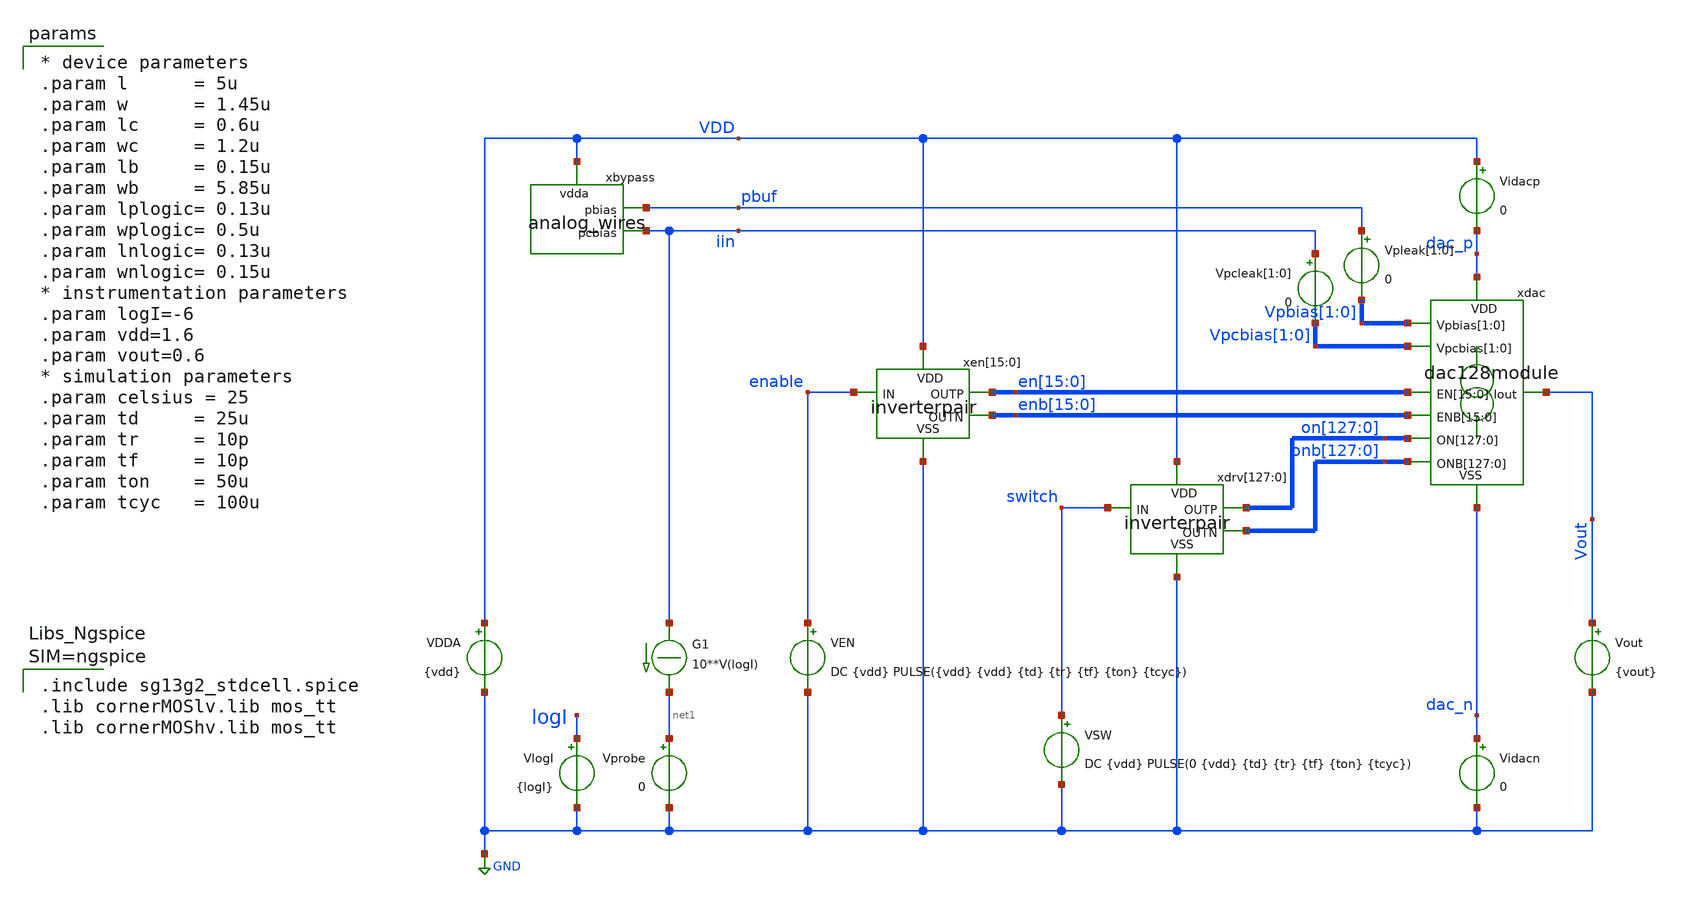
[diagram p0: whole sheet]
** sch_path: xschem/test_dac128_dc.sch
**.subckt test_dac128_dc
Vout Vout GND {vout}
.save i(vout)
Vprobe net1 GND 0
.save i(vprobe)
G1 iin net1 CUR=' 10**V(logI) '
VlogI logI GND {logI}
.save i(vlogi)
VDDA VDD GND {vdd}
.save i(vdda)
VSW switch GND DC {vdd} PULSE(0 {vdd} {td} {tr} {tf} {ton} {tcyc})
.save i(vsw)
Vidacp VDD dac_p 0
.save i(vidacp)
Vidacn dac_n GND 0
.save i(vidacn)
Vpleak[1] pbuf Vpbias[1] 0
Vpleak[0] pbuf Vpbias[0] 0
.save i(vpleak[1])
.save i(vpleak[0])
xdac dac_p en[15] en[14] en[13] en[12] en[11] en[10] en[9] en[8] en[7] en[6] en[5] en[4] en[3] en[2]
+ en[1] en[0] enb[15] enb[14] enb[13] enb[12] enb[11] enb[10] enb[9] enb[8] enb[7] enb[6] enb[5] enb[4]
+ enb[3] enb[2] enb[1] enb[0] on[127] on[126] on[125] on[124] on[123] on[122] on[121] on[120] on[119]
+ on[118] on[117] on[116] on[115] on[114] on[113] on[112] on[111] on[110] on[109] on[108] on[107] on[106]
+ on[105] on[104] on[103] on[102] on[101] on[100] on[99] on[98] on[97] on[96] on[95] on[94] on[93] on[92]
+ on[91] on[90] on[89] on[88] on[87] on[86] on[85] on[84] on[83] on[82] on[81] on[80] on[79] on[78] on[77]
+ on[76] on[75] on[74] on[73] on[72] on[71] on[70] on[69] on[68] on[67] on[66] on[65] on[64] on[63] on[62]
+ on[61] on[60] on[59] on[58] on[57] on[56] on[55] on[54] on[53] on[52] on[51] on[50] on[49] on[48] on[47]
+ on[46] on[45] on[44] on[43] on[42] on[41] on[40] on[39] on[38] on[37] on[36] on[35] on[34] on[33] on[32]
+ on[31] on[30] on[29] on[28] on[27] on[26] on[25] on[24] on[23] on[22] on[21] on[20] on[19] on[18] on[17]
+ on[16] on[15] on[14] on[13] on[12] on[11] on[10] on[9] on[8] on[7] on[6] on[5] on[4] on[3] on[2] on[1]
+ on[0] onb[127] onb[126] onb[125] onb[124] onb[123] onb[122] onb[121] onb[120] onb[119] onb[118] onb[117]
+ onb[116] onb[115] onb[114] onb[113] onb[112] onb[111] onb[110] onb[109] onb[108] onb[107] onb[106] onb[105]
+ onb[104] onb[103] onb[102] onb[101] onb[100] onb[99] onb[98] onb[97] onb[96] onb[95] onb[94] onb[93] onb[92]
+ onb[91] onb[90] onb[89] onb[88] onb[87] onb[86] onb[85] onb[84] onb[83] onb[82] onb[81] onb[80] onb[79]
+ onb[78] onb[77] onb[76] onb[75] onb[74] onb[73] onb[72] onb[71] onb[70] onb[69] onb[68] onb[67] onb[66]
+ onb[65] onb[64] onb[63] onb[62] onb[61] onb[60] onb[59] onb[58] onb[57] onb[56] onb[55] onb[54] onb[53]
+ onb[52] onb[51] onb[50] onb[49] onb[48] onb[47] onb[46] onb[45] onb[44] onb[43] onb[42] onb[41] onb[40]
+ onb[39] onb[38] onb[37] onb[36] onb[35] onb[34] onb[33] onb[32] onb[31] onb[30] onb[29] onb[28] onb[27]
+ onb[26] onb[25] onb[24] onb[23] onb[22] onb[21] onb[20] onb[19] onb[18] onb[17] onb[16] onb[15] onb[14]
+ onb[13] onb[12] onb[11] onb[10] onb[9] onb[8] onb[7] onb[6] onb[5] onb[4] onb[3] onb[2] onb[1] onb[0] Vout
+ Vpbias[1] Vpbias[0] Vpcbias[1] Vpcbias[0] dac_n dac128module
xbypass VDD pbuf iin analog_wires
Vpcleak[1] iin Vpcbias[1] 0
Vpcleak[0] iin Vpcbias[0] 0
.save i(vpcleak[1])
.save i(vpcleak[0])
xen[15] VDD en[15] enable enb[15] GND inverterpair
xen[14] VDD en[14] enable enb[14] GND inverterpair
xen[13] VDD en[13] enable enb[13] GND inverterpair
xen[12] VDD en[12] enable enb[12] GND inverterpair
xen[11] VDD en[11] enable enb[11] GND inverterpair
xen[10] VDD en[10] enable enb[10] GND inverterpair
xen[9] VDD en[9] enable enb[9] GND inverterpair
xen[8] VDD en[8] enable enb[8] GND inverterpair
xen[7] VDD en[7] enable enb[7] GND inverterpair
xen[6] VDD en[6] enable enb[6] GND inverterpair
xen[5] VDD en[5] enable enb[5] GND inverterpair
xen[4] VDD en[4] enable enb[4] GND inverterpair
xen[3] VDD en[3] enable enb[3] GND inverterpair
xen[2] VDD en[2] enable enb[2] GND inverterpair
xen[1] VDD en[1] enable enb[1] GND inverterpair
xen[0] VDD en[0] enable enb[0] GND inverterpair
xdrv[127] VDD on[127] switch onb[127] GND inverterpair
xdrv[126] VDD on[126] switch onb[126] GND inverterpair
xdrv[125] VDD on[125] switch onb[125] GND inverterpair
xdrv[124] VDD on[124] switch onb[124] GND inverterpair
xdrv[123] VDD on[123] switch onb[123] GND inverterpair
xdrv[122] VDD on[122] switch onb[122] GND inverterpair
xdrv[121] VDD on[121] switch onb[121] GND inverterpair
xdrv[120] VDD on[120] switch onb[120] GND inverterpair
xdrv[119] VDD on[119] switch onb[119] GND inverterpair
xdrv[118] VDD on[118] switch onb[118] GND inverterpair
xdrv[117] VDD on[117] switch onb[117] GND inverterpair
xdrv[116] VDD on[116] switch onb[116] GND inverterpair
xdrv[115] VDD on[115] switch onb[115] GND inverterpair
xdrv[114] VDD on[114] switch onb[114] GND inverterpair
xdrv[113] VDD on[113] switch onb[113] GND inverterpair
xdrv[112] VDD on[112] switch onb[112] GND inverterpair
xdrv[111] VDD on[111] switch onb[111] GND inverterpair
xdrv[110] VDD on[110] switch onb[110] GND inverterpair
xdrv[109] VDD on[109] switch onb[109] GND inverterpair
xdrv[108] VDD on[108] switch onb[108] GND inverterpair
xdrv[107] VDD on[107] switch onb[107] GND inverterpair
xdrv[106] VDD on[106] switch onb[106] GND inverterpair
xdrv[105] VDD on[105] switch onb[105] GND inverterpair
xdrv[104] VDD on[104] switch onb[104] GND inverterpair
xdrv[103] VDD on[103] switch onb[103] GND inverterpair
xdrv[102] VDD on[102] switch onb[102] GND inverterpair
xdrv[101] VDD on[101] switch onb[101] GND inverterpair
xdrv[100] VDD on[100] switch onb[100] GND inverterpair
xdrv[99] VDD on[99] switch onb[99] GND inverterpair
xdrv[98] VDD on[98] switch onb[98] GND inverterpair
xdrv[97] VDD on[97] switch onb[97] GND inverterpair
xdrv[96] VDD on[96] switch onb[96] GND inverterpair
xdrv[95] VDD on[95] switch onb[95] GND inverterpair
xdrv[94] VDD on[94] switch onb[94] GND inverterpair
xdrv[93] VDD on[93] switch onb[93] GND inverterpair
xdrv[92] VDD on[92] switch onb[92] GND inverterpair
xdrv[91] VDD on[91] switch onb[91] GND inverterpair
xdrv[90] VDD on[90] switch onb[90] GND inverterpair
xdrv[89] VDD on[89] switch onb[89] GND inverterpair
xdrv[88] VDD on[88] switch onb[88] GND inverterpair
xdrv[87] VDD on[87] switch onb[87] GND inverterpair
xdrv[86] VDD on[86] switch onb[86] GND inverterpair
xdrv[85] VDD on[85] switch onb[85] GND inverterpair
xdrv[84] VDD on[84] switch onb[84] GND inverterpair
xdrv[83] VDD on[83] switch onb[83] GND inverterpair
xdrv[82] VDD on[82] switch onb[82] GND inverterpair
xdrv[81] VDD on[81] switch onb[81] GND inverterpair
xdrv[80] VDD on[80] switch onb[80] GND inverterpair
xdrv[79] VDD on[79] switch onb[79] GND inverterpair
xdrv[78] VDD on[78] switch onb[78] GND inverterpair
xdrv[77] VDD on[77] switch onb[77] GND inverterpair
xdrv[76] VDD on[76] switch onb[76] GND inverterpair
xdrv[75] VDD on[75] switch onb[75] GND inverterpair
xdrv[74] VDD on[74] switch onb[74] GND inverterpair
xdrv[73] VDD on[73] switch onb[73] GND inverterpair
xdrv[72] VDD on[72] switch onb[72] GND inverterpair
xdrv[71] VDD on[71] switch onb[71] GND inverterpair
xdrv[70] VDD on[70] switch onb[70] GND inverterpair
xdrv[69] VDD on[69] switch onb[69] GND inverterpair
xdrv[68] VDD on[68] switch onb[68] GND inverterpair
xdrv[67] VDD on[67] switch onb[67] GND inverterpair
xdrv[66] VDD on[66] switch onb[66] GND inverterpair
xdrv[65] VDD on[65] switch onb[65] GND inverterpair
xdrv[64] VDD on[64] switch onb[64] GND inverterpair
xdrv[63] VDD on[63] switch onb[63] GND inverterpair
xdrv[62] VDD on[62] switch onb[62] GND inverterpair
xdrv[61] VDD on[61] switch onb[61] GND inverterpair
xdrv[60] VDD on[60] switch onb[60] GND inverterpair
xdrv[59] VDD on[59] switch onb[59] GND inverterpair
xdrv[58] VDD on[58] switch onb[58] GND inverterpair
xdrv[57] VDD on[57] switch onb[57] GND inverterpair
xdrv[56] VDD on[56] switch onb[56] GND inverterpair
xdrv[55] VDD on[55] switch onb[55] GND inverterpair
xdrv[54] VDD on[54] switch onb[54] GND inverterpair
xdrv[53] VDD on[53] switch onb[53] GND inverterpair
xdrv[52] VDD on[52] switch onb[52] GND inverterpair
xdrv[51] VDD on[51] switch onb[51] GND inverterpair
xdrv[50] VDD on[50] switch onb[50] GND inverterpair
xdrv[49] VDD on[49] switch onb[49] GND inverterpair
xdrv[48] VDD on[48] switch onb[48] GND inverterpair
xdrv[47] VDD on[47] switch onb[47] GND inverterpair
xdrv[46] VDD on[46] switch onb[46] GND inverterpair
xdrv[45] VDD on[45] switch onb[45] GND inverterpair
xdrv[44] VDD on[44] switch onb[44] GND inverterpair
xdrv[43] VDD on[43] switch onb[43] GND inverterpair
xdrv[42] VDD on[42] switch onb[42] GND inverterpair
xdrv[41] VDD on[41] switch onb[41] GND inverterpair
xdrv[40] VDD on[40] switch onb[40] GND inverterpair
xdrv[39] VDD on[39] switch onb[39] GND inverterpair
xdrv[38] VDD on[38] switch onb[38] GND inverterpair
xdrv[37] VDD on[37] switch onb[37] GND inverterpair
xdrv[36] VDD on[36] switch onb[36] GND inverterpair
xdrv[35] VDD on[35] switch onb[35] GND inverterpair
xdrv[34] VDD on[34] switch onb[34] GND inverterpair
xdrv[33] VDD on[33] switch onb[33] GND inverterpair
xdrv[32] VDD on[32] switch onb[32] GND inverterpair
xdrv[31] VDD on[31] switch onb[31] GND inverterpair
xdrv[30] VDD on[30] switch onb[30] GND inverterpair
xdrv[29] VDD on[29] switch onb[29] GND inverterpair
xdrv[28] VDD on[28] switch onb[28] GND inverterpair
xdrv[27] VDD on[27] switch onb[27] GND inverterpair
xdrv[26] VDD on[26] switch onb[26] GND inverterpair
xdrv[25] VDD on[25] switch onb[25] GND inverterpair
xdrv[24] VDD on[24] switch onb[24] GND inverterpair
xdrv[23] VDD on[23] switch onb[23] GND inverterpair
xdrv[22] VDD on[22] switch onb[22] GND inverterpair
xdrv[21] VDD on[21] switch onb[21] GND inverterpair
xdrv[20] VDD on[20] switch onb[20] GND inverterpair
xdrv[19] VDD on[19] switch onb[19] GND inverterpair
xdrv[18] VDD on[18] switch onb[18] GND inverterpair
xdrv[17] VDD on[17] switch onb[17] GND inverterpair
xdrv[16] VDD on[16] switch onb[16] GND inverterpair
xdrv[15] VDD on[15] switch onb[15] GND inverterpair
xdrv[14] VDD on[14] switch onb[14] GND inverterpair
xdrv[13] VDD on[13] switch onb[13] GND inverterpair
xdrv[12] VDD on[12] switch onb[12] GND inverterpair
xdrv[11] VDD on[11] switch onb[11] GND inverterpair
xdrv[10] VDD on[10] switch onb[10] GND inverterpair
xdrv[9] VDD on[9] switch onb[9] GND inverterpair
xdrv[8] VDD on[8] switch onb[8] GND inverterpair
xdrv[7] VDD on[7] switch onb[7] GND inverterpair
xdrv[6] VDD on[6] switch onb[6] GND inverterpair
xdrv[5] VDD on[5] switch onb[5] GND inverterpair
xdrv[4] VDD on[4] switch onb[4] GND inverterpair
xdrv[3] VDD on[3] switch onb[3] GND inverterpair
xdrv[2] VDD on[2] switch onb[2] GND inverterpair
xdrv[1] VDD on[1] switch onb[1] GND inverterpair
xdrv[0] VDD on[0] switch onb[0] GND inverterpair
VEN enable GND DC {vdd} PULSE({vdd} {vdd} {td} {tr} {tf} {ton} {tcyc})
.save i(ven)
**** begin user architecture code


.include test_dac128_dc.save
.temp=27
.options gmin=1e-15 abstol=1p method=gear
.options savecurrents
.control
save all
op
write test_dac128_dc.raw
set appendwrite
dc Vout 0 1.6 10m VlogI -7 -5 0.5
*tran 10n 500u
write test_dac128_dc.raw
plot 2*(vout#branch-8*vprobe#branch)/(8*vprobe#branch+vout#branch)
plot vdd pbuf iin enable switch v("en[0]") v("enb[0]") v("on[0]") v("onb[0]") Vout
plot vout#branch vprobe#branch
*plot @n.xsw.xmbias.nsg13_lv_pmos[ids] @n.xsw.xmpullup.nsg13_lv_pmos[ids]
plot vidacp#branch vidacn#branch
*plot 0.5*(vidacp#branch+vidacn#branch) vidacp#branch-vidacn#branch
.endc




.include sg13g2_stdcell.spice
.lib cornerMOSlv.lib mos_tt
.lib cornerMOShv.lib mos_tt



* device parameters
.param l      = 5u
.param w      = 1.45u
.param lc     = 0.6u
.param wc     = 1.2u
.param lb     = 0.15u
.param wb     = 5.85u
.param lplogic= 0.13u
.param wplogic= 0.5u
.param lnlogic= 0.13u
.param wnlogic= 0.15u
* instrumentation parameters
.param logI=-6
.param vdd=1.6
.param vout=0.6
* simulation parameters
.param celsius = 25
.param td     = 25u
.param tr     = 10p
.param tf     = 10p
.param ton    = 50u
.param tcyc   = 100u


**** end user architecture code
**.ends

* expanding   symbol:  dac128module.sym # of pins=9
** sym_path: xschem/dac128module.sym
** sch_path: xschem/dac128module.sch
.subckt dac128module VDD EN[15] EN[14] EN[13] EN[12] EN[11] EN[10] EN[9] EN[8] EN[7] EN[6] EN[5]
+ EN[4] EN[3] EN[2] EN[1] EN[0] ENB[15] ENB[14] ENB[13] ENB[12] ENB[11] ENB[10] ENB[9] ENB[8] ENB[7] ENB[6]
+ ENB[5] ENB[4] ENB[3] ENB[2] ENB[1] ENB[0] ON[127] ON[126] ON[125] ON[124] ON[123] ON[122] ON[121] ON[120]
+ ON[119] ON[118] ON[117] ON[116] ON[115] ON[114] ON[113] ON[112] ON[111] ON[110] ON[109] ON[108] ON[107]
+ ON[106] ON[105] ON[104] ON[103] ON[102] ON[101] ON[100] ON[99] ON[98] ON[97] ON[96] ON[95] ON[94] ON[93]
+ ON[92] ON[91] ON[90] ON[89] ON[88] ON[87] ON[86] ON[85] ON[84] ON[83] ON[82] ON[81] ON[80] ON[79] ON[78]
+ ON[77] ON[76] ON[75] ON[74] ON[73] ON[72] ON[71] ON[70] ON[69] ON[68] ON[67] ON[66] ON[65] ON[64] ON[63]
+ ON[62] ON[61] ON[60] ON[59] ON[58] ON[57] ON[56] ON[55] ON[54] ON[53] ON[52] ON[51] ON[50] ON[49] ON[48]
+ ON[47] ON[46] ON[45] ON[44] ON[43] ON[42] ON[41] ON[40] ON[39] ON[38] ON[37] ON[36] ON[35] ON[34] ON[33]
+ ON[32] ON[31] ON[30] ON[29] ON[28] ON[27] ON[26] ON[25] ON[24] ON[23] ON[22] ON[21] ON[20] ON[19] ON[18]
+ ON[17] ON[16] ON[15] ON[14] ON[13] ON[12] ON[11] ON[10] ON[9] ON[8] ON[7] ON[6] ON[5] ON[4] ON[3] ON[2]
+ ON[1] ON[0] ONB[127] ONB[126] ONB[125] ONB[124] ONB[123] ONB[122] ONB[121] ONB[120] ONB[119] ONB[118]
+ ONB[117] ONB[116] ONB[115] ONB[114] ONB[113] ONB[112] ONB[111] ONB[110] ONB[109] ONB[108] ONB[107] ONB[106]
+ ONB[105] ONB[104] ONB[103] ONB[102] ONB[101] ONB[100] ONB[99] ONB[98] ONB[97] ONB[96] ONB[95] ONB[94]
+ ONB[93] ONB[92] ONB[91] ONB[90] ONB[89] ONB[88] ONB[87] ONB[86] ONB[85] ONB[84] ONB[83] ONB[82] ONB[81]
+ ONB[80] ONB[79] ONB[78] ONB[77] ONB[76] ONB[75] ONB[74] ONB[73] ONB[72] ONB[71] ONB[70] ONB[69] ONB[68]
+ ONB[67] ONB[66] ONB[65] ONB[64] ONB[63] ONB[62] ONB[61] ONB[60] ONB[59] ONB[58] ONB[57] ONB[56] ONB[55]
+ ONB[54] ONB[53] ONB[52] ONB[51] ONB[50] ONB[49] ONB[48] ONB[47] ONB[46] ONB[45] ONB[44] ONB[43] ONB[42]
+ ONB[41] ONB[40] ONB[39] ONB[38] ONB[37] ONB[36] ONB[35] ONB[34] ONB[33] ONB[32] ONB[31] ONB[30] ONB[29]
+ ONB[28] ONB[27] ONB[26] ONB[25] ONB[24] ONB[23] ONB[22] ONB[21] ONB[20] ONB[19] ONB[18] ONB[17] ONB[16]
+ ONB[15] ONB[14] ONB[13] ONB[12] ONB[11] ONB[10] ONB[9] ONB[8] ONB[7] ONB[6] ONB[5] ONB[4] ONB[3] ONB[2]
+ ONB[1] ONB[0] Iout Vpbias[1] Vpbias[0] Vpcbias[1] Vpcbias[0] VSS
*.opin Iout
*.ipin
*+ ON[127],ON[126],ON[125],ON[124],ON[123],ON[122],ON[121],ON[120],ON[119],ON[118],ON[117],ON[116],ON[115],ON[114],ON[113],ON[112],ON[111],ON[110],ON[109],ON[108],ON[107],ON[106],ON[105],ON[104],ON[103],ON[102],ON[101],ON[100],ON[99],ON[98],ON[97],ON[96],ON[95],ON[94],ON[93],ON[92],ON[91],ON[90],ON[89],ON[88],ON[87],ON[86],ON[85],ON[84],ON[83],ON[82],ON[81],ON[80],ON[79],ON[78],ON[77],ON[76],ON[75],ON[74],ON[73],ON[72],ON[71],ON[70],ON[69],ON[68],ON[67],ON[66],ON[65],ON[64],ON[63],ON[62],ON[61],ON[60],ON[59],ON[58],ON[57],ON[56],ON[55],ON[54],ON[53],ON[52],ON[51],ON[50],ON[49],ON[48],ON[47],ON[46],ON[45],ON[44],ON[43],ON[42],ON[41],ON[40],ON[39],ON[38],ON[37],ON[36],ON[35],ON[34],ON[33],ON[32],ON[31],ON[30],ON[29],ON[28],ON[27],ON[26],ON[25],ON[24],ON[23],ON[22],ON[21],ON[20],ON[19],ON[18],ON[17],ON[16],ON[15],ON[14],ON[13],ON[12],ON[11],ON[10],ON[9],ON[8],ON[7],ON[6],ON[5],ON[4],ON[3],ON[2],ON[1],ON[0]
*.ipin
*+ ONB[127],ONB[126],ONB[125],ONB[124],ONB[123],ONB[122],ONB[121],ONB[120],ONB[119],ONB[118],ONB[117],ONB[116],ONB[115],ONB[114],ONB[113],ONB[112],ONB[111],ONB[110],ONB[109],ONB[108],ONB[107],ONB[106],ONB[105],ONB[104],ONB[103],ONB[102],ONB[101],ONB[100],ONB[99],ONB[98],ONB[97],ONB[96],ONB[95],ONB[94],ONB[93],ONB[92],ONB[91],ONB[90],ONB[89],ONB[88],ONB[87],ONB[86],ONB[85],ONB[84],ONB[83],ONB[82],ONB[81],ONB[80],ONB[79],ONB[78],ONB[77],ONB[76],ONB[75],ONB[74],ONB[73],ONB[72],ONB[71],ONB[70],ONB[69],ONB[68],ONB[67],ONB[66],ONB[65],ONB[64],ONB[63],ONB[62],ONB[61],ONB[60],ONB[59],ONB[58],ONB[57],ONB[56],ONB[55],ONB[54],ONB[53],ONB[52],ONB[51],ONB[50],ONB[49],ONB[48],ONB[47],ONB[46],ONB[45],ONB[44],ONB[43],ONB[42],ONB[41],ONB[40],ONB[39],ONB[38],ONB[37],ONB[36],ONB[35],ONB[34],ONB[33],ONB[32],ONB[31],ONB[30],ONB[29],ONB[28],ONB[27],ONB[26],ONB[25],ONB[24],ONB[23],ONB[22],ONB[21],ONB[20],ONB[19],ONB[18],ONB[17],ONB[16],ONB[15],ONB[14],ONB[13],ONB[12],ONB[11],ONB[10],ONB[9],ONB[8],ONB[7],ONB[6],ONB[5],ONB[4],ONB[3],ONB[2],ONB[1],ONB[0]
*.iopin VSS
*.iopin VDD
*.iopin Vpcbias[1],Vpcbias[0]
*.ipin
*+ EN[15],EN[14],EN[13],EN[12],EN[11],EN[10],EN[9],EN[8],EN[7],EN[6],EN[5],EN[4],EN[3],EN[2],EN[1],EN[0]
*.ipin
*+ ENB[15],ENB[14],ENB[13],ENB[12],ENB[11],ENB[10],ENB[9],ENB[8],ENB[7],ENB[6],ENB[5],ENB[4],ENB[3],ENB[2],ENB[1],ENB[0]
*.iopin Vpbias[1],Vpbias[0]
XMcbias[0] Vpcbias[0] Vpcbias[0] Vpbias[0] VDD sg13_lv_pmos w=5.85u l=0.15u ng=1 m=8 mm_ok=1
**** begin user architecture code

* device parameters
.param l      = 5u
.param w      = 1.45u
.param lc     = 0.6u
.param wc     = 1.2u
.param lb     = 0.15u
.param wb     = 5.85u
.param lplogic= 0.13u
.param wplogic= 0.5u
.param lnlogic= 0.13u
.param wnlogic= 0.15u


**** end user architecture code
xref[7] VDD Vpbias[0] EN[7] ENB[7] Vpbias[0] Vpcbias[0] VSS unitsource2u
xref[6] VDD Vpbias[0] EN[6] ENB[6] Vpbias[0] Vpcbias[0] VSS unitsource2u
xref[5] VDD Vpbias[0] EN[5] ENB[5] Vpbias[0] Vpcbias[0] VSS unitsource2u
xref[4] VDD Vpbias[0] EN[4] ENB[4] Vpbias[0] Vpcbias[0] VSS unitsource2u
xref[3] VDD Vpbias[0] EN[3] ENB[3] Vpbias[0] Vpcbias[0] VSS unitsource2u
xref[2] VDD Vpbias[0] EN[2] ENB[2] Vpbias[0] Vpcbias[0] VSS unitsource2u
xref[1] VDD Vpbias[0] EN[1] ENB[1] Vpbias[0] Vpcbias[0] VSS unitsource2u
xref[0] VDD Vpbias[0] EN[0] ENB[0] Vpbias[0] Vpcbias[0] VSS unitsource2u
xsrc[63] VDD net1 ON[63] ONB[63] Iout net2 VSS unitsource2u
xsrc[62] VDD net1 ON[62] ONB[62] Iout net2 VSS unitsource2u
xsrc[61] VDD net1 ON[61] ONB[61] Iout net2 VSS unitsource2u
xsrc[60] VDD net1 ON[60] ONB[60] Iout net2 VSS unitsource2u
xsrc[59] VDD net1 ON[59] ONB[59] Iout net2 VSS unitsource2u
xsrc[58] VDD net1 ON[58] ONB[58] Iout net2 VSS unitsource2u
xsrc[57] VDD net1 ON[57] ONB[57] Iout net2 VSS unitsource2u
xsrc[56] VDD net1 ON[56] ONB[56] Iout net2 VSS unitsource2u
xsrc[55] VDD net1 ON[55] ONB[55] Iout net2 VSS unitsource2u
xsrc[54] VDD net1 ON[54] ONB[54] Iout net2 VSS unitsource2u
xsrc[53] VDD net1 ON[53] ONB[53] Iout net2 VSS unitsource2u
xsrc[52] VDD net1 ON[52] ONB[52] Iout net2 VSS unitsource2u
xsrc[51] VDD net1 ON[51] ONB[51] Iout net2 VSS unitsource2u
xsrc[50] VDD net1 ON[50] ONB[50] Iout net2 VSS unitsource2u
xsrc[49] VDD net1 ON[49] ONB[49] Iout net2 VSS unitsource2u
xsrc[48] VDD net1 ON[48] ONB[48] Iout net2 VSS unitsource2u
xsrc[47] VDD net1 ON[47] ONB[47] Iout net2 VSS unitsource2u
xsrc[46] VDD net1 ON[46] ONB[46] Iout net2 VSS unitsource2u
xsrc[45] VDD net1 ON[45] ONB[45] Iout net2 VSS unitsource2u
xsrc[44] VDD net1 ON[44] ONB[44] Iout net2 VSS unitsource2u
xsrc[43] VDD net1 ON[43] ONB[43] Iout net2 VSS unitsource2u
xsrc[42] VDD net1 ON[42] ONB[42] Iout net2 VSS unitsource2u
xsrc[41] VDD net1 ON[41] ONB[41] Iout net2 VSS unitsource2u
xsrc[40] VDD net1 ON[40] ONB[40] Iout net2 VSS unitsource2u
xsrc[39] VDD net1 ON[39] ONB[39] Iout net2 VSS unitsource2u
xsrc[38] VDD net1 ON[38] ONB[38] Iout net2 VSS unitsource2u
xsrc[37] VDD net1 ON[37] ONB[37] Iout net2 VSS unitsource2u
xsrc[36] VDD net1 ON[36] ONB[36] Iout net2 VSS unitsource2u
xsrc[35] VDD net1 ON[35] ONB[35] Iout net2 VSS unitsource2u
xsrc[34] VDD net1 ON[34] ONB[34] Iout net2 VSS unitsource2u
xsrc[33] VDD net1 ON[33] ONB[33] Iout net2 VSS unitsource2u
xsrc[32] VDD net1 ON[32] ONB[32] Iout net2 VSS unitsource2u
xsrc[31] VDD net1 ON[31] ONB[31] Iout net2 VSS unitsource2u
xsrc[30] VDD net1 ON[30] ONB[30] Iout net2 VSS unitsource2u
xsrc[29] VDD net1 ON[29] ONB[29] Iout net2 VSS unitsource2u
xsrc[28] VDD net1 ON[28] ONB[28] Iout net2 VSS unitsource2u
xsrc[27] VDD net1 ON[27] ONB[27] Iout net2 VSS unitsource2u
xsrc[26] VDD net1 ON[26] ONB[26] Iout net2 VSS unitsource2u
xsrc[25] VDD net1 ON[25] ONB[25] Iout net2 VSS unitsource2u
xsrc[24] VDD net1 ON[24] ONB[24] Iout net2 VSS unitsource2u
xsrc[23] VDD net1 ON[23] ONB[23] Iout net2 VSS unitsource2u
xsrc[22] VDD net1 ON[22] ONB[22] Iout net2 VSS unitsource2u
xsrc[21] VDD net1 ON[21] ONB[21] Iout net2 VSS unitsource2u
xsrc[20] VDD net1 ON[20] ONB[20] Iout net2 VSS unitsource2u
xsrc[19] VDD net1 ON[19] ONB[19] Iout net2 VSS unitsource2u
xsrc[18] VDD net1 ON[18] ONB[18] Iout net2 VSS unitsource2u
xsrc[17] VDD net1 ON[17] ONB[17] Iout net2 VSS unitsource2u
xsrc[16] VDD net1 ON[16] ONB[16] Iout net2 VSS unitsource2u
xsrc[15] VDD net1 ON[15] ONB[15] Iout net2 VSS unitsource2u
xsrc[14] VDD net1 ON[14] ONB[14] Iout net2 VSS unitsource2u
xsrc[13] VDD net1 ON[13] ONB[13] Iout net2 VSS unitsource2u
xsrc[12] VDD net1 ON[12] ONB[12] Iout net2 VSS unitsource2u
xsrc[11] VDD net1 ON[11] ONB[11] Iout net2 VSS unitsource2u
xsrc[10] VDD net1 ON[10] ONB[10] Iout net2 VSS unitsource2u
xsrc[9] VDD net1 ON[9] ONB[9] Iout net2 VSS unitsource2u
xsrc[8] VDD net1 ON[8] ONB[8] Iout net2 VSS unitsource2u
xsrc[7] VDD net1 ON[7] ONB[7] Iout net2 VSS unitsource2u
xsrc[6] VDD net1 ON[6] ONB[6] Iout net2 VSS unitsource2u
xsrc[5] VDD net1 ON[5] ONB[5] Iout net2 VSS unitsource2u
xsrc[4] VDD net1 ON[4] ONB[4] Iout net2 VSS unitsource2u
xsrc[3] VDD net1 ON[3] ONB[3] Iout net2 VSS unitsource2u
xsrc[2] VDD net1 ON[2] ONB[2] Iout net2 VSS unitsource2u
xsrc[1] VDD net1 ON[1] ONB[1] Iout net2 VSS unitsource2u
xsrc[0] VDD net1 ON[0] ONB[0] Iout net2 VSS unitsource2u
XMcbias[1] Vpcbias[1] Vpcbias[1] Vpbias[1] VDD sg13_lv_pmos w=5.85u l=0.15u ng=1 m=8 mm_ok=1
xref1[15] VDD Vpbias[1] EN[15] ENB[15] Vpbias[1] Vpcbias[1] VSS unitsource2u
xref1[14] VDD Vpbias[1] EN[14] ENB[14] Vpbias[1] Vpcbias[1] VSS unitsource2u
xref1[13] VDD Vpbias[1] EN[13] ENB[13] Vpbias[1] Vpcbias[1] VSS unitsource2u
xref1[12] VDD Vpbias[1] EN[12] ENB[12] Vpbias[1] Vpcbias[1] VSS unitsource2u
xref1[11] VDD Vpbias[1] EN[11] ENB[11] Vpbias[1] Vpcbias[1] VSS unitsource2u
xref1[10] VDD Vpbias[1] EN[10] ENB[10] Vpbias[1] Vpcbias[1] VSS unitsource2u
xref1[9] VDD Vpbias[1] EN[9] ENB[9] Vpbias[1] Vpcbias[1] VSS unitsource2u
xref1[8] VDD Vpbias[1] EN[8] ENB[8] Vpbias[1] Vpcbias[1] VSS unitsource2u
xsrc1[127] VDD net4 ON[127] ONB[127] Iout net3 VSS unitsource2u
xsrc1[126] VDD net4 ON[126] ONB[126] Iout net3 VSS unitsource2u
xsrc1[125] VDD net4 ON[125] ONB[125] Iout net3 VSS unitsource2u
xsrc1[124] VDD net4 ON[124] ONB[124] Iout net3 VSS unitsource2u
xsrc1[123] VDD net4 ON[123] ONB[123] Iout net3 VSS unitsource2u
xsrc1[122] VDD net4 ON[122] ONB[122] Iout net3 VSS unitsource2u
xsrc1[121] VDD net4 ON[121] ONB[121] Iout net3 VSS unitsource2u
xsrc1[120] VDD net4 ON[120] ONB[120] Iout net3 VSS unitsource2u
xsrc1[119] VDD net4 ON[119] ONB[119] Iout net3 VSS unitsource2u
xsrc1[118] VDD net4 ON[118] ONB[118] Iout net3 VSS unitsource2u
xsrc1[117] VDD net4 ON[117] ONB[117] Iout net3 VSS unitsource2u
xsrc1[116] VDD net4 ON[116] ONB[116] Iout net3 VSS unitsource2u
xsrc1[115] VDD net4 ON[115] ONB[115] Iout net3 VSS unitsource2u
xsrc1[114] VDD net4 ON[114] ONB[114] Iout net3 VSS unitsource2u
xsrc1[113] VDD net4 ON[113] ONB[113] Iout net3 VSS unitsource2u
xsrc1[112] VDD net4 ON[112] ONB[112] Iout net3 VSS unitsource2u
xsrc1[111] VDD net4 ON[111] ONB[111] Iout net3 VSS unitsource2u
xsrc1[110] VDD net4 ON[110] ONB[110] Iout net3 VSS unitsource2u
xsrc1[109] VDD net4 ON[109] ONB[109] Iout net3 VSS unitsource2u
xsrc1[108] VDD net4 ON[108] ONB[108] Iout net3 VSS unitsource2u
xsrc1[107] VDD net4 ON[107] ONB[107] Iout net3 VSS unitsource2u
xsrc1[106] VDD net4 ON[106] ONB[106] Iout net3 VSS unitsource2u
xsrc1[105] VDD net4 ON[105] ONB[105] Iout net3 VSS unitsource2u
xsrc1[104] VDD net4 ON[104] ONB[104] Iout net3 VSS unitsource2u
xsrc1[103] VDD net4 ON[103] ONB[103] Iout net3 VSS unitsource2u
xsrc1[102] VDD net4 ON[102] ONB[102] Iout net3 VSS unitsource2u
xsrc1[101] VDD net4 ON[101] ONB[101] Iout net3 VSS unitsource2u
xsrc1[100] VDD net4 ON[100] ONB[100] Iout net3 VSS unitsource2u
xsrc1[99] VDD net4 ON[99] ONB[99] Iout net3 VSS unitsource2u
xsrc1[98] VDD net4 ON[98] ONB[98] Iout net3 VSS unitsource2u
xsrc1[97] VDD net4 ON[97] ONB[97] Iout net3 VSS unitsource2u
xsrc1[96] VDD net4 ON[96] ONB[96] Iout net3 VSS unitsource2u
xsrc1[95] VDD net4 ON[95] ONB[95] Iout net3 VSS unitsource2u
xsrc1[94] VDD net4 ON[94] ONB[94] Iout net3 VSS unitsource2u
xsrc1[93] VDD net4 ON[93] ONB[93] Iout net3 VSS unitsource2u
xsrc1[92] VDD net4 ON[92] ONB[92] Iout net3 VSS unitsource2u
xsrc1[91] VDD net4 ON[91] ONB[91] Iout net3 VSS unitsource2u
xsrc1[90] VDD net4 ON[90] ONB[90] Iout net3 VSS unitsource2u
xsrc1[89] VDD net4 ON[89] ONB[89] Iout net3 VSS unitsource2u
xsrc1[88] VDD net4 ON[88] ONB[88] Iout net3 VSS unitsource2u
xsrc1[87] VDD net4 ON[87] ONB[87] Iout net3 VSS unitsource2u
xsrc1[86] VDD net4 ON[86] ONB[86] Iout net3 VSS unitsource2u
xsrc1[85] VDD net4 ON[85] ONB[85] Iout net3 VSS unitsource2u
xsrc1[84] VDD net4 ON[84] ONB[84] Iout net3 VSS unitsource2u
xsrc1[83] VDD net4 ON[83] ONB[83] Iout net3 VSS unitsource2u
xsrc1[82] VDD net4 ON[82] ONB[82] Iout net3 VSS unitsource2u
xsrc1[81] VDD net4 ON[81] ONB[81] Iout net3 VSS unitsource2u
xsrc1[80] VDD net4 ON[80] ONB[80] Iout net3 VSS unitsource2u
xsrc1[79] VDD net4 ON[79] ONB[79] Iout net3 VSS unitsource2u
xsrc1[78] VDD net4 ON[78] ONB[78] Iout net3 VSS unitsource2u
xsrc1[77] VDD net4 ON[77] ONB[77] Iout net3 VSS unitsource2u
xsrc1[76] VDD net4 ON[76] ONB[76] Iout net3 VSS unitsource2u
xsrc1[75] VDD net4 ON[75] ONB[75] Iout net3 VSS unitsource2u
xsrc1[74] VDD net4 ON[74] ONB[74] Iout net3 VSS unitsource2u
xsrc1[73] VDD net4 ON[73] ONB[73] Iout net3 VSS unitsource2u
xsrc1[72] VDD net4 ON[72] ONB[72] Iout net3 VSS unitsource2u
xsrc1[71] VDD net4 ON[71] ONB[71] Iout net3 VSS unitsource2u
xsrc1[70] VDD net4 ON[70] ONB[70] Iout net3 VSS unitsource2u
xsrc1[69] VDD net4 ON[69] ONB[69] Iout net3 VSS unitsource2u
xsrc1[68] VDD net4 ON[68] ONB[68] Iout net3 VSS unitsource2u
xsrc1[67] VDD net4 ON[67] ONB[67] Iout net3 VSS unitsource2u
xsrc1[66] VDD net4 ON[66] ONB[66] Iout net3 VSS unitsource2u
xsrc1[65] VDD net4 ON[65] ONB[65] Iout net3 VSS unitsource2u
xsrc1[64] VDD net4 ON[64] ONB[64] Iout net3 VSS unitsource2u
* tap: EN[15:0] --> EN[7:0]
* tap: ENB[15:0] --> ENB[7:0]
* tap: ENB[15:0] --> ENB[15:8]
* tap: EN[15:0] --> EN[15:8]
* tap: ON[127:0] --> ON[63:0]
* tap: ONB[127:0] --> ONB[63:0]
* tap: ON[127:0] --> ON[127:64]
* tap: ONB[127:0] --> ONB[127:64]
* tap: Vpbias[1:0] --> Vpbias[0]
* tap: Vpcbias[1:0] --> Vpcbias[0]
* tap: Vpbias[1:0] --> Vpbias[1]
* tap: Vpcbias[1:0] --> Vpcbias[1]
E1 VDD net1 VDD Vpbias[0] 1
E2 VDD net2 VDD Vpcbias[0] 1
E3 VDD net4 VDD Vpbias[1] 1
E4 VDD net3 VDD Vpcbias[1] 1
.ends


* expanding   symbol:  analog_wires.sym # of pins=3
** sym_path: xschem/analog_wires.sym
** sch_path: xschem/analog_wires.sch
.subckt analog_wires vdda pbias pcbias
*.iopin vdda
*.iopin pcbias
*.iopin pbias
XMcbuffer vdda pcbias vdda vdda sg13_hv_pmos w=8u l=8u ng=1 m=19 mm_ok=1
XMbbuffer vdda pbias vdda vdda sg13_hv_pmos w=8u l=8u ng=1 m=19 mm_ok=1
.ends


* expanding   symbol:  inverterpair.sym # of pins=5
** sym_path: xschem/inverterpair.sym
** sch_path: xschem/inverterpair.sch
.subckt inverterpair VDD OUTP IN OUTN VSS
*.iopin VSS
*.ipin IN
*.opin OUTN
*.opin OUTP
*.iopin VDD
xinv2 OUTP OUTN VDD VSS sg13g2_inv_1
xinv1 OUTN IN VDD VSS sg13g2_inv_1
.ends


* expanding   symbol:  unitsource2u.sym # of pins=7
** sym_path: xschem/unitsource2u.sym
** sch_path: xschem/unitsource2u.sch
.subckt unitsource2u VDD VbiasP ON ONB Iout VcascP VSS
*.iopin VSS
*.iopin VDD
*.iopin VbiasP
*.iopin VcascP
*.ipin ON
*.ipin ONB
*.iopin Iout
xnonoverlap VDD VSS ON ONB on_n off_n nonoverlap
xsw VDD off_n Vcasc on_n VcascP cascodeswitch_pmos
xsrc VDD VbiasP Vcasc Iout pcsource2u
.ends


* expanding   symbol:  sg13g2_stdcells/sg13g2_inv_1.sym # of pins=2
** sym_path: sg13g2_stdcells/sg13g2_inv_1.sym
** sch_path: sg13g2_stdcells/sg13g2_inv_1.sch
.subckt sg13g2_inv_1 Y A VDD VSS
*.opin Y
*.ipin A
*.iopin VDD
*.iopin VSS
XM1 Y A VSS VSS sg13_lv_nmos w=740.00n l=130.00n ng=1 m=1 mm_ok=1
XM2 Y A VDD VDD sg13_lv_pmos w=1.12u l=130.00n ng=1 m=1 mm_ok=1
.ends


* expanding   symbol:  nonoverlap.sym # of pins=6
** sym_path: xschem/nonoverlap.sym
** sch_path: xschem/nonoverlap.sch
.subckt nonoverlap VDD VSS INP INN OUTN OUTP
*.iopin VSS
*.iopin VDD
*.ipin INP
*.ipin INN
*.opin OUTP
*.opin OUTN
XM1 OUTN INP VDD VDD sg13_lv_pmos w=0.3u l=0.13u ng=1 m=1 mm_ok=1
XM2 OUTP INN VDD VDD sg13_lv_pmos w=0.3u l=0.13u ng=1 m=1 mm_ok=1
XM3 OUTN OUTP VSS VSS sg13_lv_nmos w=0.15u l=0.52u ng=1 m=1 mm_ok=1
XM4 OUTP OUTN VSS VSS sg13_lv_nmos w=0.15u l=0.52u ng=1 m=1 mm_ok=1
.ends


* expanding   symbol:  cascodeswitch_pmos.sym # of pins=5
** sym_path: xschem/cascodeswitch_pmos.sym
** sch_path: xschem/cascodeswitch_pmos.sch
.subckt cascodeswitch_pmos VDD off_n Vcasc on_n Vbpcasc
*.ipin off_n
*.ipin Vbpcasc
*.opin Vcasc
*.ipin on_n
*.ipin VDD
XMpullup Vcasc off_n VDD VDD sg13_lv_pmos w=0.3u l=0.13u ng=1 m=1 mm_ok=1
XMbias Vbpcasc on_n Vcasc VDD sg13_lv_pmos w=0.3u l=0.13u ng=1 m=1 mm_ok=1
.ends


* expanding   symbol:  pcsource2u.sym # of pins=4
** sym_path: xschem/pcsource2u.sym
** sch_path: xschem/pcsource2u.sch
.subckt pcsource2u VDD VbiasP VcascodeP Iout
*.ipin VcascodeP
*.ipin VbiasP
*.opin Iout
*.ipin VDD
XMsrc drain net4 VDD net1 sg13_lv_pmos w=1.45u l=5u ng=1 m=1 mm_ok=1
XMcasc Iout net3 drain net2 sg13_lv_pmos w=1.2u l=0.6u ng=1 m=1 mm_ok=1
Vgsrc net4 VbiasP 0
.save i(vgsrc)
Vgcasc net3 VcascodeP 0
.save i(vgcasc)
Vbsrc VDD net1 0
.save i(vbsrc)
Vbcasc VDD net2 0
.save i(vbcasc)
.ends

.GLOBAL GND
.end
